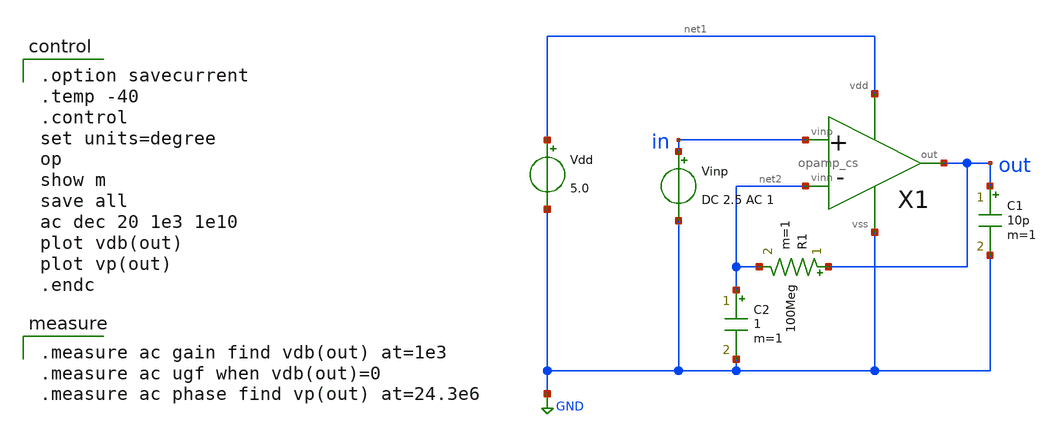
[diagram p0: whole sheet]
** sch_path: OR1/PTC06/opamp/opamp_cs_ac_temp.sch
**.subckt opamp_cs_ac_temp
Vdd net1 GND 5.0
Vinp in GND DC 2.5 AC 1
C1 out GND 10p m=1
R1 out net2 100Meg m=1
C2 net2 GND 1 m=1
X1 in net2 out net1 GND opamp_cs
**** begin user architecture code

.option savecurrent
.temp -40
.control
set units=degree
op
show m
save all
ac dec 20 1e3 1e10
plot vdb(out)
plot vp(out)
.endc


.measure ac gain find vdb(out) at=1e3
.measure ac ugf when vdb(out)=0
.measure ac phase find vp(out) at=24.3e6

 .include $::LIB/mos.lib
.include $::LIB/passive.lib
.include $::LIB/diode.lib
**** end user architecture code
**.ends

* expanding   symbol:  opamp_cs.sym # of pins=5
** sym_path: OR1/PTC06/opamp/opamp_cs.sym
** sch_path: OR1/PTC06/opamp/opamp_cs.sch
.subckt opamp_cs vinp vinn out vdd vss
*.ipin vinp
*.ipin vinn
*.opin out
*.iopin vdd
*.iopin vss
X1 vinp vinn net2 vdd vss net5 diff
X2 net2 net5 out vdd vss cs
M3 net5 net5 vdd vdd pmos L=2u W=20u m=1
C1 out net3 poly_cap W=18 L=18
M2 net3 net1 net2 vss nmos L=2u W=40u m=1
M6 net1 net5 vdd vdd pmos L=2u W=20u m=1
M1 net1 net1 net4 vss nmos L=2u W=10u m=1
M7 net4 net4 vss vss nmos L=2u W=10u m=1
x3 vdd net7 vss cs-vth-ref_sym
M4 net6 net7 vdd vdd pmos L=2u W=20u m=1
M5 net6 net6 vss vss nmos L=2u W=5u m=1
M8 net5 net6 vss vss nmos L=2u W=5u m=1
.ends


* expanding   symbol:  diff.sym # of pins=6
** sym_path: diff.sym
** sch_path: diff.sch
.subckt diff vinp vinn out vdd vss vb
*.ipin vinn
*.ipin vinp
*.ipin vb
*.opin out
*.iopin vdd
*.iopin vss
M5 net2 vb vdd vdd pmos L=2u W=40u m=1
M1 net1 vinn net2 net2 pmos L=2u W=200u m=1
M2 out vinp net2 net2 pmos L=2u W=200u m=1
M3 net1 net1 vss vss nmos L=2u W=10u m=1
M4 out net1 vss vss nmos L=2u W=10u m=1
.ends


* expanding   symbol:  cs.sym # of pins=5
** sym_path: cs.sym
** sch_path: cs.sch
.subckt cs vin vb out vdd vss
*.ipin vb
*.ipin vin
*.opin out
*.iopin vss
*.iopin vdd
M6 out vb vdd vdd pmos L=2u W=400u m=1
M7 out vin vss vss nmos L=2u W=200u m=1
.ends


* expanding   symbol:  cs-vth-ref_sym.sym # of pins=3
** sym_path: cs-vth-ref_sym.sym
** sch_path: cs-vth-ref_sym.sch
.subckt cs-vth-ref_sym vdd ib vss
*.iopin vdd
*.iopin vss
*.iopin ib
R2 vss net2 HR_poly W=2.0 L=2000
M4 ib ib vdd vdd pmos L=2u W=100u m=1
M3 net1 ib vdd vdd pmos L=2u W=100u m=1
M2 ib net1 net2 vss nmos L=2u W=20u m=1
M1 net1 net2 vss vss nmos L=2u W=20u m=1
.ends

.GLOBAL GND
.end
